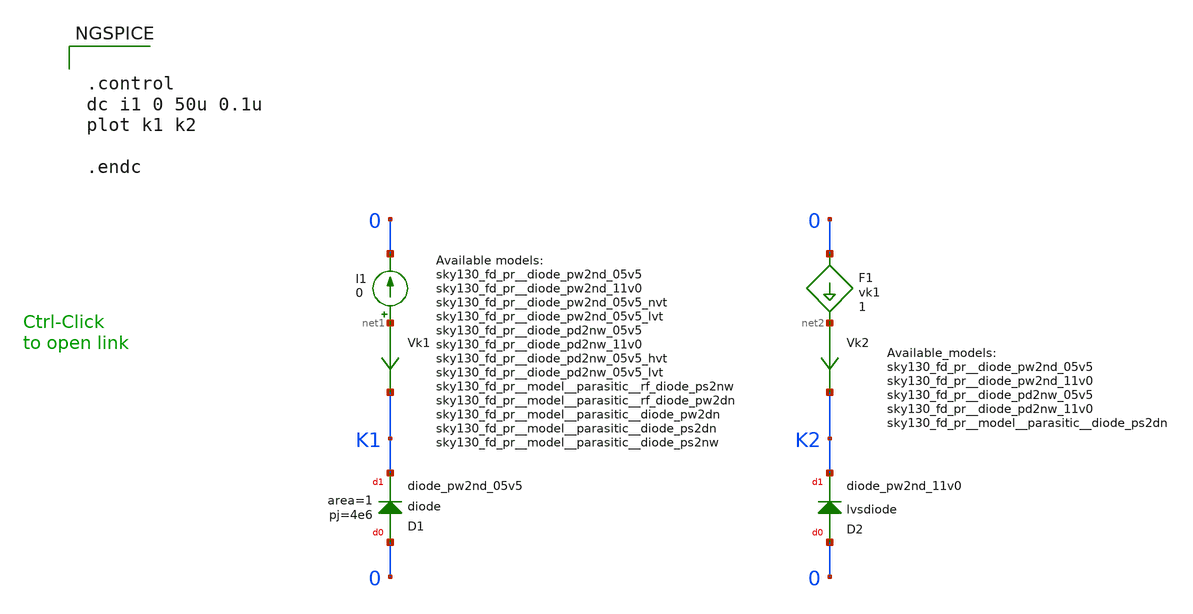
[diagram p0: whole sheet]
** sch_path: sky130_tests/test_diode.sch
* Copyright 2020 Stefan Frederik Schippers
* Licensed under the Apache License, Version 2.0 (the "License");
* you may not use this file except in compliance with the License.
* You may obtain a copy of the License at
* https://www.apache.org/licenses/LICENSE-2.0
* Unless required by applicable law or agreed to in writing, software
* distributed under the License is distributed on an "AS IS" BASIS,
* WITHOUT WARRANTIES OR CONDITIONS OF ANY KIND, either express or implied.
* See the License for the specific language governing permissions and
* limitations under the License.
**.subckt test_diode
I1 net1 0 0
Vk1 net1 K1 0
.save i(vk1)
XD1 0 K1 sky130_fd_pr__diode_pw2nd_05v5 area=1 pj=4e6
Vk2 net2 K2 0
.save i(vk2)
D2 0 K2 sky130_fd_pr__diode_pw2nd_11v0 area=1
F1 0 net2 vk1 1
**** begin user architecture code


.control
dc i1 0 50u 0.1u
plot k1 k2

.endc



**** end user architecture code
**.ends
.end
